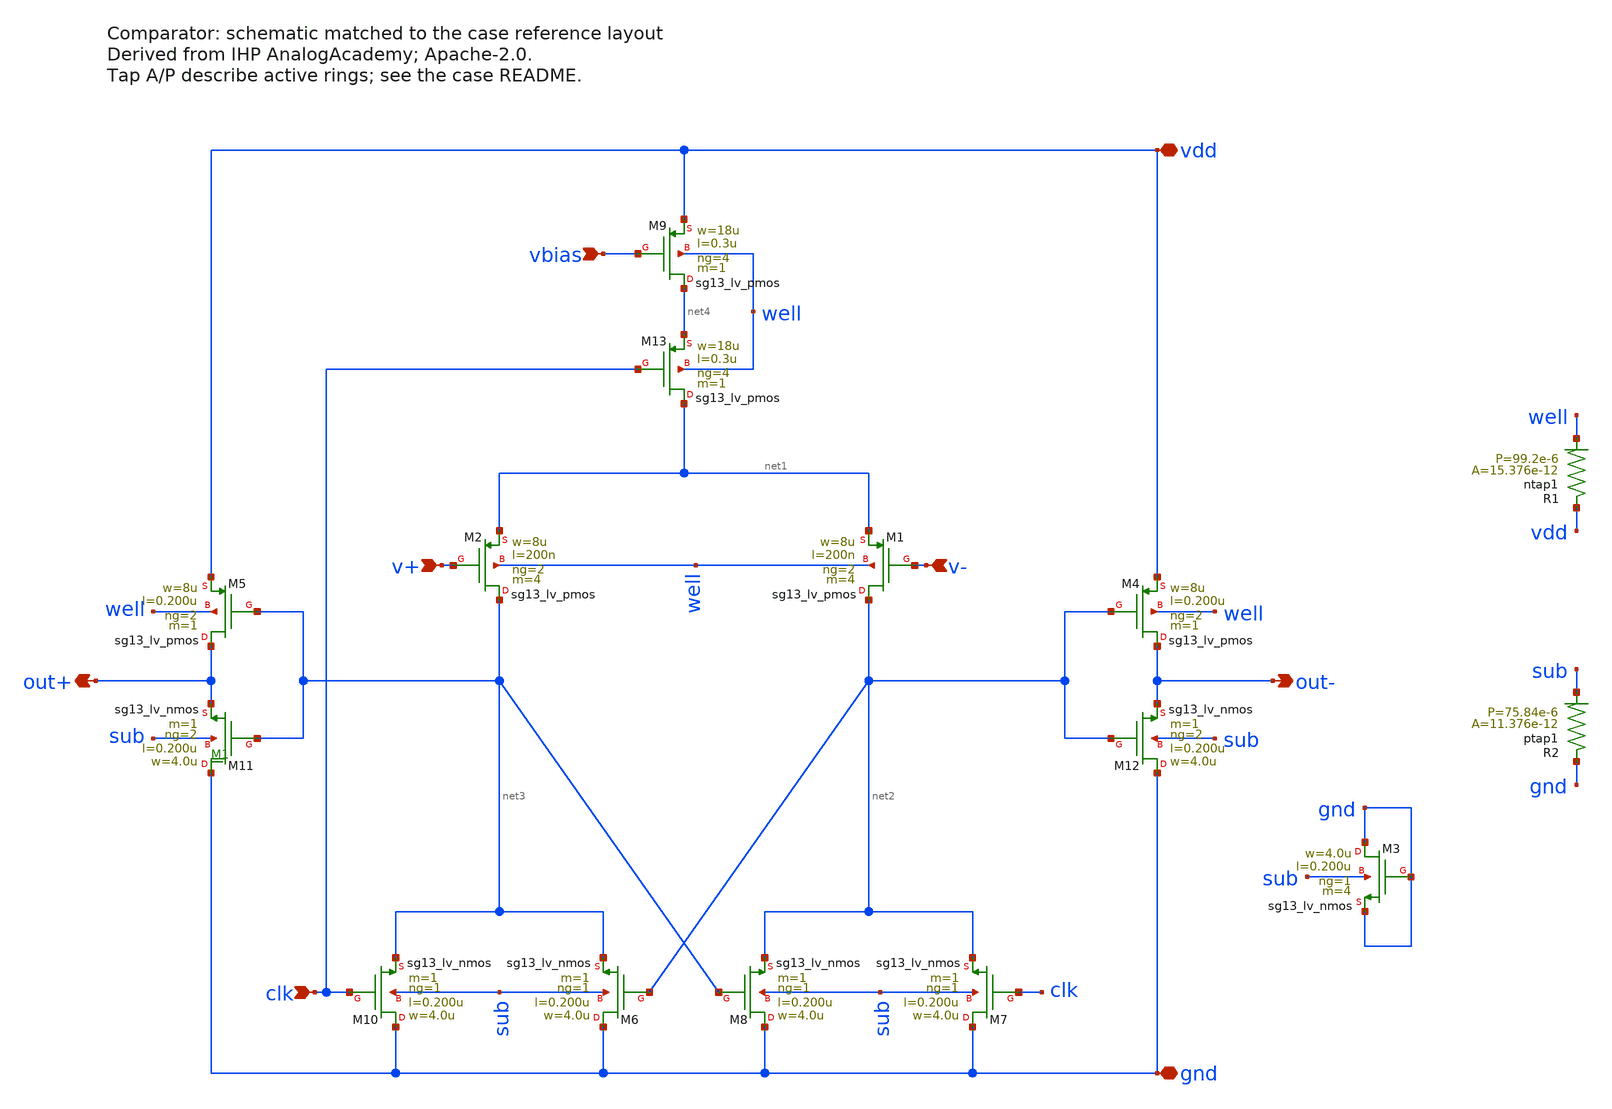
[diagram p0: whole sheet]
** sch_path: tasks/IHP-AnalogAcademy/cases/comparator/source/DIFF_COMPARATOR.sch
**.subckt DIFF_COMPARATOR vdd gnd v+ v- clk out- out+ vbias
*.iopin vdd
*.iopin gnd
*.ipin v+
*.ipin v-
*.ipin clk
*.opin out-
*.opin out+
*.ipin vbias
XM2 net3 v+ net1 well sg13_lv_pmos w=8u l=200n ng=2 m=4 mm_ok=1
XM1 net2 v- net1 well sg13_lv_pmos w=8u l=200n ng=2 m=4 mm_ok=1
XM4 out- net2 vdd well sg13_lv_pmos w=8u l=0.200u ng=2 m=1 mm_ok=1
XM5 out+ net3 vdd well sg13_lv_pmos w=8u l=0.200u ng=2 m=1 mm_ok=1
XM11 gnd net3 out+ sub sg13_lv_nmos w=4.0u l=0.200u ng=2 m=1 mm_ok=1
XM12 gnd net2 out- sub sg13_lv_nmos w=4.0u l=0.200u ng=2 m=1 mm_ok=1
XM6 gnd net2 net3 sub sg13_lv_nmos w=4.0u l=0.200u ng=1 m=1 mm_ok=1
XM10 gnd clk net3 sub sg13_lv_nmos w=4.0u l=0.200u ng=1 m=1 mm_ok=1
XM7 gnd clk net2 sub sg13_lv_nmos w=4.0u l=0.200u ng=1 m=1 mm_ok=1
XM8 gnd net3 net2 sub sg13_lv_nmos w=4.0u l=0.200u ng=1 m=1 mm_ok=1
XM3 gnd gnd gnd sub sg13_lv_nmos w=4.0u l=0.200u ng=1 m=4 mm_ok=1
XM13 net1 clk net4 well sg13_lv_pmos w=18u l=0.3u ng=4 m=1 mm_ok=1
XM9 net4 vbias vdd well sg13_lv_pmos w=18u l=0.3u ng=4 m=1 mm_ok=1
XR1 vdd well ntap1 a=15.376e-12 p=99.2e-6 r=8.553
XR2 gnd sub ptap1 a=11.376e-12 p=75.84e-6 r=11.24
**.ends
.end
